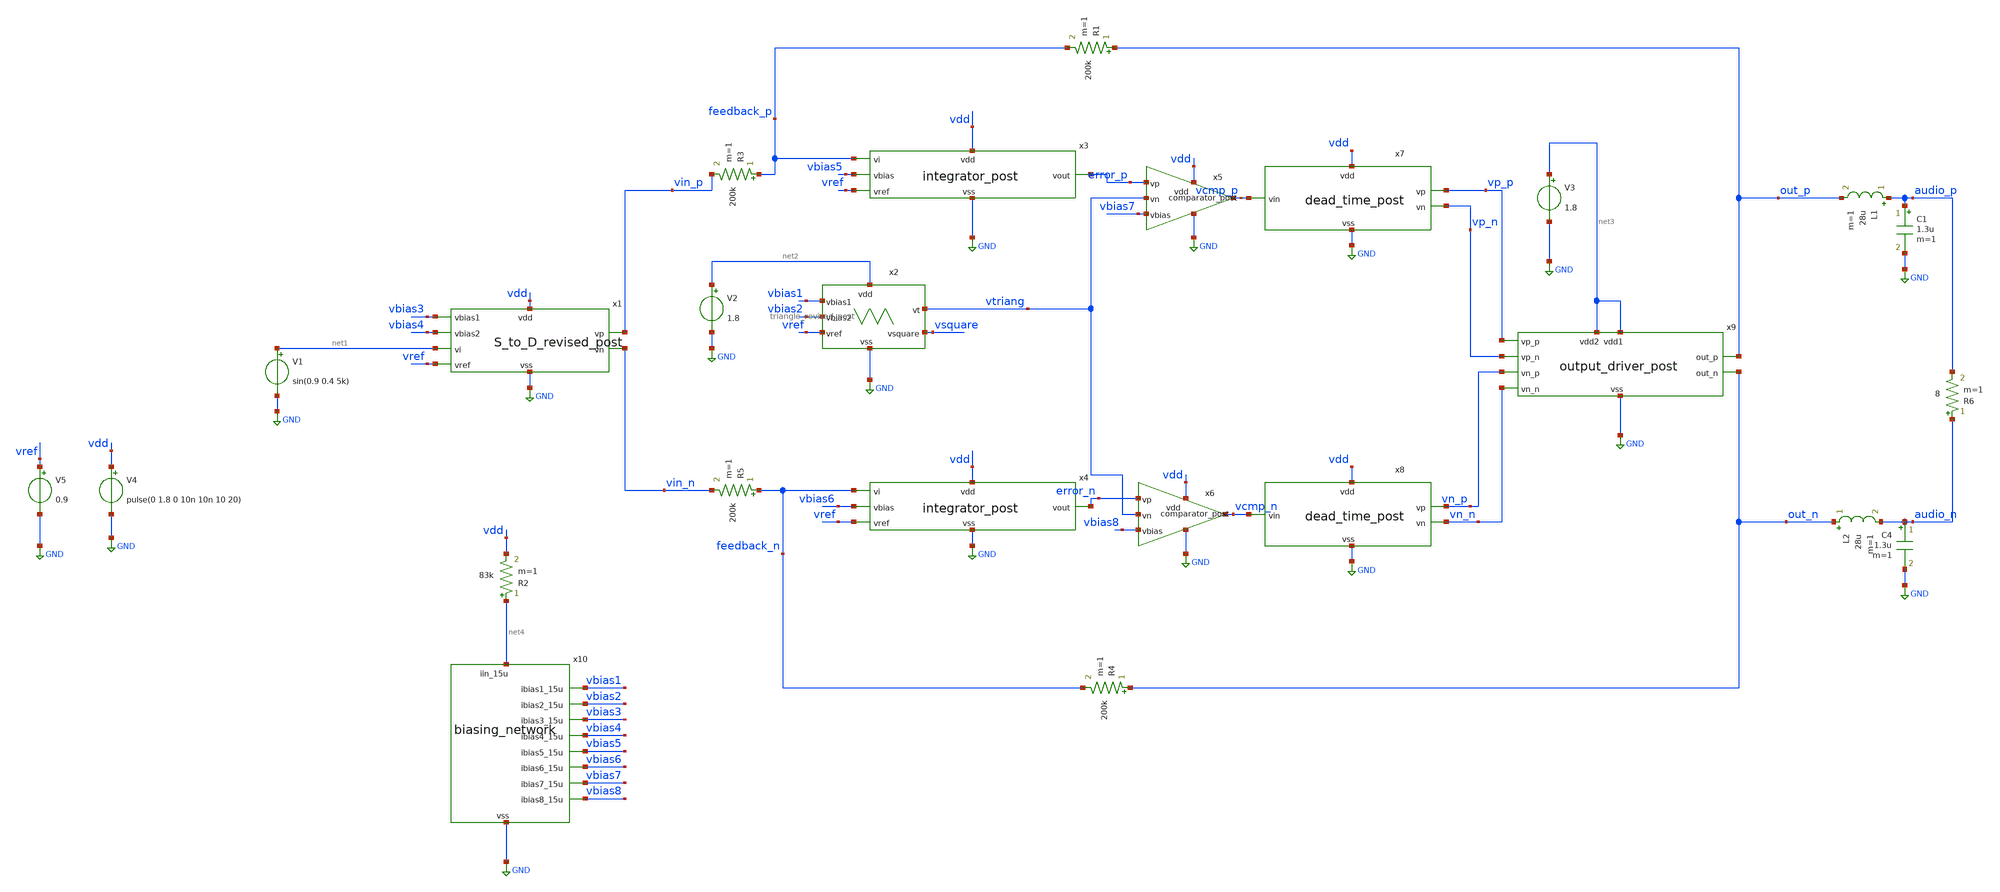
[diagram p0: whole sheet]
** sch_path: xschem/src/Class_D/Class_D_revised_tb_2.sch
**.subckt Class_D_revised_tb_2
V1 net1 GND sin(0.9 0.4 5k)
V5 vref GND 0.9
L1 audio_p out_p 28u m=1
C1 audio_p GND 1.3u m=1
R1 out_p feedback_p 200k m=1
R3 feedback_p vin_p 200k m=1
R4 out_n feedback_n 200k m=1
R5 feedback_n vin_n 200k m=1
L2 out_n audio_n 28u m=1
C4 audio_n GND 1.3u m=1
R6 audio_n audio_p 8 m=1
V4 vdd GND pulse(0 1.8 0 10n 10n 10 20)
V2 net2 GND 1.8
x9 net3 vp_p out_p GND vp_n vn_p out_n vn_n net3 output_driver_post
V3 net3 GND 1.8
x7 vdd vcmp_p vp_p vp_n GND dead_time_post
x8 vdd vcmp_n vn_p vn_n GND dead_time_post
x5 vdd error_p vtriang vbias7 GND vcmp_p comparator_post
x6 vdd error_n vtriang vbias8 GND vcmp_n comparator_post
x3 vdd feedback_p vbias5 vref GND error_p integrator_post
x4 vdd feedback_n vbias6 vref GND error_n integrator_post
x1 vdd vbias3 vbias4 net1 vref GND vin_n vin_p S_to_D_revised_post
x2 net2 vbias1 vbias2 vref GND vsquare vtriang triangle_revised_post
x10 net4 vbias1 vbias2 vbias3 vbias4 vbias5 vbias6 vbias7 vbias8 GND biasing_network
R2 net4 vdd 83k m=1
**** begin user architecture code


.option rshunt=1e20
.nodeset V(audio_p)=0.9 V(audio_n)=0.9 V(vp_p)=0.79 V(vn_p)=0 V(vcmp_p)=0.859  V(vp_n)=0.79
+ V(vn_n)=0 V(vcmp_n)=0.859 v(vin_p)=0.9 v(vin_n)=0.9 v(vtriang)=0.9
*.nodeset all=0.9
*.option VNTOL=1e-6 ABSTOL=1e-9
*.option savecurrents
*set the absolute voltage error tolerance and absolute current error tolerance
.control
save out_p out_n audio_p audio_n I(V4) I(V2) @r6[i] @r1[i] i(v3) i(v6) vtriang vin_p vin_n error_p
+ error_n vcmp_p vcmp_n vp_p vp_n vn_p vn_n
*save vtriang audio_p audio_n I(V2) @r6[i] out_p out_n
*op
tran 3n 10m 0.1m
*linearize V(audio)
*linearize V(out)
*fft V(out)
*fft V(audio)
*plot mag(V(audio))
*plot mag(V(out))
let pout=@r6[i]*(V(audio_p)-V(audio_n))
let pin=1.8*(I(V4)+I(V2)+I(V3))
meas tran pload avg pout from=2m to=9m
meas tran p_supply avg pin from=2m to=9m
*print pload/p_supply
set nfreqs=20
*fourier 10k V(out_p)-V(out_n)

fourier 5k V(audio_p)-V(audio_n)
write class_d_5k_04_post_notflat.raw

.endc





.include /home/eda/pdk/skywater-pdk/libraries/sky130_fd_pr_ngspice/latest/models/corners/tt.spice
.include /home/eda/magic/class_d_audio_amplifier/OTA/OTA_int_post.spice
.include /home/eda/magic/class_d_audio_amplifier/OTA/OTA_post.spice
.include /home/eda/magic/class_d_audio_amplifier/S_to_D/S_to_D_post.spice
.include /home/eda/magic/class_d_audio_amplifier/S_to_D/S_to_D_revised_post.spice
.include /home/eda/magic/class_d_audio_amplifier/triang/triangle_post.spice
.include /home/eda/magic/class_d_audio_amplifier/triang/triangle_revised_post.spice
.include /home/eda/magic/class_d_audio_amplifier/comparator/comparator_post.spice
.include /home/eda/magic/class_d_audio_amplifier/dead_time/dead_time_post.spice
.include /home/eda/magic/class_d_audio_amplifier/output_driver/output_driver_post_r.spice
.include /home/eda/magic/class_d_audio_amplifier/integrator/integrator_post.spice
.include /home/eda/magic/class_d_audio_amplifier/biasing_network.spice
* Resistor$::SKYWATER_MODELS/Capacitor
.include $::SKYWATER_MODELS/models/r+c/res_typical__cap_typical.spice
.include $::SKYWATER_MODELS/models/r+c/res_typical__cap_typical__lin.spice
* Special cells
.include $::SKYWATER_MODELS/models/corners/tt/specialized_cells.spice


**** end user architecture code
**.ends

* expanding   symbol:  src/biasing_network/biasing_network.sym # of pins=10
** sym_path: xschem/src/biasing_network/biasing_network.sym
** sch_path: xschem/src/biasing_network/biasing_network.sch
.subckt biasing_network iin_15u ibias1_15u ibias2_15u ibias3_15u ibias4_15u ibias5_15u ibias6_15u
+ ibias7_15u ibias8_15u vss
*.iopin iin_15u
*.iopin vss
*.opin ibias1_15u
*.opin ibias2_15u
*.opin ibias3_15u
*.opin ibias4_15u
*.opin ibias5_15u
*.opin ibias6_15u
*.opin ibias7_15u
*.opin ibias8_15u
XM5 iin_15u iin_15u vss vss sky130_fd_pr__nfet_01v8_lvt L=2 W=4 nf=2 ad='int((nf+1)/2) * W/nf * 0.29'
+ as='int((nf+2)/2) * W/nf * 0.29' pd='2*int((nf+1)/2) * (W/nf + 0.29)' ps='2*int((nf+2)/2) * (W/nf + 0.29)'
+ nrd='0.29 / W' nrs='0.29 / W' sa=0 sb=0 sd=0 mult=8 m=8
XM6 ibias1_15u iin_15u vss vss sky130_fd_pr__nfet_01v8_lvt L=2 W=4 nf=2 ad='int((nf+1)/2) * W/nf * 0.29'
+ as='int((nf+2)/2) * W/nf * 0.29' pd='2*int((nf+1)/2) * (W/nf + 0.29)' ps='2*int((nf+2)/2) * (W/nf + 0.29)'
+ nrd='0.29 / W' nrs='0.29 / W' sa=0 sb=0 sd=0 mult=8 m=8
XM7 ibias2_15u iin_15u vss vss sky130_fd_pr__nfet_01v8_lvt L=2 W=4 nf=2 ad='int((nf+1)/2) * W/nf * 0.29'
+ as='int((nf+2)/2) * W/nf * 0.29' pd='2*int((nf+1)/2) * (W/nf + 0.29)' ps='2*int((nf+2)/2) * (W/nf + 0.29)'
+ nrd='0.29 / W' nrs='0.29 / W' sa=0 sb=0 sd=0 mult=8 m=8
XM8 ibias3_15u iin_15u vss vss sky130_fd_pr__nfet_01v8_lvt L=2 W=4 nf=2 ad='int((nf+1)/2) * W/nf * 0.29'
+ as='int((nf+2)/2) * W/nf * 0.29' pd='2*int((nf+1)/2) * (W/nf + 0.29)' ps='2*int((nf+2)/2) * (W/nf + 0.29)'
+ nrd='0.29 / W' nrs='0.29 / W' sa=0 sb=0 sd=0 mult=8 m=8
XM9 ibias4_15u iin_15u vss vss sky130_fd_pr__nfet_01v8_lvt L=2 W=4 nf=2 ad='int((nf+1)/2) * W/nf * 0.29'
+ as='int((nf+2)/2) * W/nf * 0.29' pd='2*int((nf+1)/2) * (W/nf + 0.29)' ps='2*int((nf+2)/2) * (W/nf + 0.29)'
+ nrd='0.29 / W' nrs='0.29 / W' sa=0 sb=0 sd=0 mult=8 m=8
XM10 ibias5_15u iin_15u vss vss sky130_fd_pr__nfet_01v8_lvt L=2 W=4 nf=2 ad='int((nf+1)/2) * W/nf * 0.29'
+ as='int((nf+2)/2) * W/nf * 0.29' pd='2*int((nf+1)/2) * (W/nf + 0.29)' ps='2*int((nf+2)/2) * (W/nf + 0.29)'
+ nrd='0.29 / W' nrs='0.29 / W' sa=0 sb=0 sd=0 mult=8 m=8
XM11 ibias6_15u iin_15u vss vss sky130_fd_pr__nfet_01v8_lvt L=2 W=4 nf=2 ad='int((nf+1)/2) * W/nf * 0.29'
+ as='int((nf+2)/2) * W/nf * 0.29' pd='2*int((nf+1)/2) * (W/nf + 0.29)' ps='2*int((nf+2)/2) * (W/nf + 0.29)'
+ nrd='0.29 / W' nrs='0.29 / W' sa=0 sb=0 sd=0 mult=8 m=8
XM12 vss iin_15u ibias7_15u vss sky130_fd_pr__nfet_01v8_lvt L=2 W=4 nf=2 ad='int((nf+1)/2) * W/nf * 0.29'
+ as='int((nf+2)/2) * W/nf * 0.29' pd='2*int((nf+1)/2) * (W/nf + 0.29)' ps='2*int((nf+2)/2) * (W/nf + 0.29)'
+ nrd='0.29 / W' nrs='0.29 / W' sa=0 sb=0 sd=0 mult=8 m=8
XM13 ibias8_15u iin_15u vss vss sky130_fd_pr__nfet_01v8_lvt L=2 W=4 nf=2 ad='int((nf+1)/2) * W/nf * 0.29'
+ as='int((nf+2)/2) * W/nf * 0.29' pd='2*int((nf+1)/2) * (W/nf + 0.29)' ps='2*int((nf+2)/2) * (W/nf + 0.29)'
+ nrd='0.29 / W' nrs='0.29 / W' sa=0 sb=0 sd=0 mult=8 m=8
.ends

.GLOBAL GND
.end
